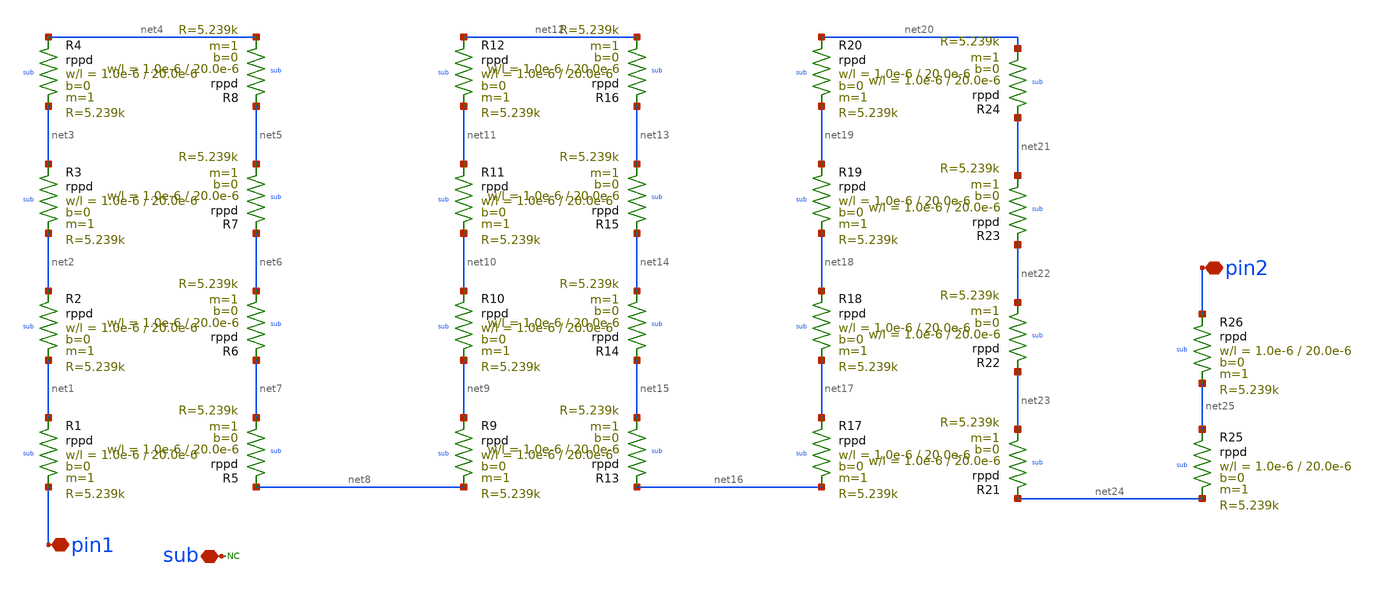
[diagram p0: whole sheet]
** sch_path: designs/libs/sg13g2_io/xschem/sg13g2_RCClampResistor.sch
**.subckt sg13g2_RCClampResistor pin1 pin2 sub
*.iopin pin1
*.iopin pin2
*.iopin sub
XR1 net1 pin1 sub rppd w=1.0e-6 l=20.0e-6 m=1 b=0 mm_ok=1
XR2 net2 net1 sub rppd w=1.0e-6 l=20.0e-6 m=1 b=0 mm_ok=1
XR3 net3 net2 sub rppd w=1.0e-6 l=20.0e-6 m=1 b=0 mm_ok=1
XR4 net4 net3 sub rppd w=1.0e-6 l=20.0e-6 m=1 b=0 mm_ok=1
XR5 net8 net7 sub rppd w=1.0e-6 l=20.0e-6 m=1 b=0 mm_ok=1
XR6 net7 net6 sub rppd w=1.0e-6 l=20.0e-6 m=1 b=0 mm_ok=1
XR7 net6 net5 sub rppd w=1.0e-6 l=20.0e-6 m=1 b=0 mm_ok=1
XR8 net5 net4 sub rppd w=1.0e-6 l=20.0e-6 m=1 b=0 mm_ok=1
XR9 net9 net8 sub rppd w=1.0e-6 l=20.0e-6 m=1 b=0 mm_ok=1
XR10 net10 net9 sub rppd w=1.0e-6 l=20.0e-6 m=1 b=0 mm_ok=1
XR11 net11 net10 sub rppd w=1.0e-6 l=20.0e-6 m=1 b=0 mm_ok=1
XR12 net12 net11 sub rppd w=1.0e-6 l=20.0e-6 m=1 b=0 mm_ok=1
XR13 net16 net15 sub rppd w=1.0e-6 l=20.0e-6 m=1 b=0 mm_ok=1
XR14 net15 net14 sub rppd w=1.0e-6 l=20.0e-6 m=1 b=0 mm_ok=1
XR15 net14 net13 sub rppd w=1.0e-6 l=20.0e-6 m=1 b=0 mm_ok=1
XR16 net13 net12 sub rppd w=1.0e-6 l=20.0e-6 m=1 b=0 mm_ok=1
XR17 net17 net16 sub rppd w=1.0e-6 l=20.0e-6 m=1 b=0 mm_ok=1
XR18 net18 net17 sub rppd w=1.0e-6 l=20.0e-6 m=1 b=0 mm_ok=1
XR19 net19 net18 sub rppd w=1.0e-6 l=20.0e-6 m=1 b=0 mm_ok=1
XR20 net20 net19 sub rppd w=1.0e-6 l=20.0e-6 m=1 b=0 mm_ok=1
XR21 net24 net23 sub rppd w=1.0e-6 l=20.0e-6 m=1 b=0 mm_ok=1
XR22 net23 net22 sub rppd w=1.0e-6 l=20.0e-6 m=1 b=0 mm_ok=1
XR23 net22 net21 sub rppd w=1.0e-6 l=20.0e-6 m=1 b=0 mm_ok=1
XR24 net21 net20 sub rppd w=1.0e-6 l=20.0e-6 m=1 b=0 mm_ok=1
XR25 net25 net24 sub rppd w=1.0e-6 l=20.0e-6 m=1 b=0 mm_ok=1
XR26 pin2 net25 sub rppd w=1.0e-6 l=20.0e-6 m=1 b=0 mm_ok=1
* noconn sub
**.ends
.end
